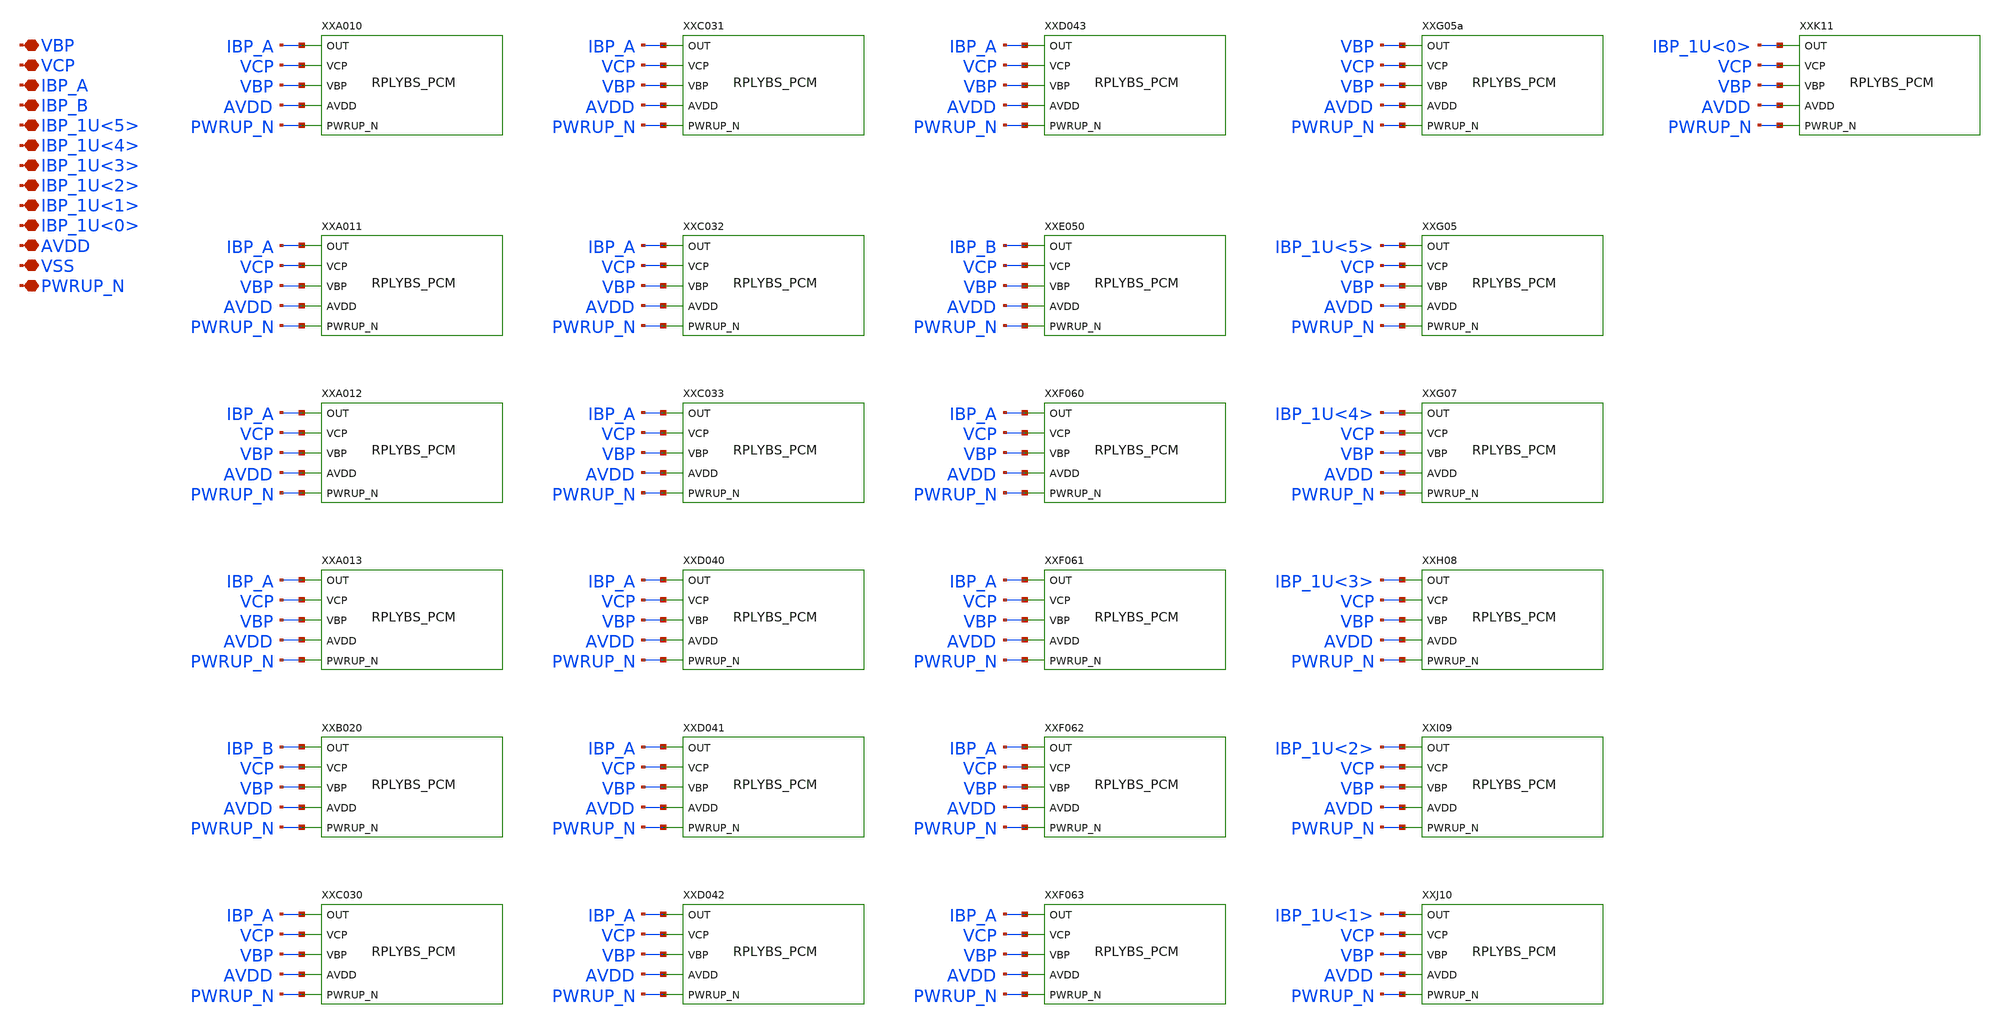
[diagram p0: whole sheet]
** sch_path: design/RPLY_BIAS_SKY130NM/RPLYBS_PMIRR.sch
**.subckt RPLYBS_PMIRR VBP VCP IBP_A IBP_B IBP_1U<5> IBP_1U<4> IBP_1U<3> IBP_1U<2> IBP_1U<1>
*+ IBP_1U<0> AVDD VSS PWRUP_N
*.iopin VBP
*.iopin VCP
*.iopin IBP_A
*.iopin IBP_B
*.iopin IBP_1U<5>
*.iopin IBP_1U<4>
*.iopin IBP_1U<3>
*.iopin IBP_1U<2>
*.iopin IBP_1U<1>
*.iopin IBP_1U<0>
*.iopin AVDD
*.iopin VSS
*.iopin PWRUP_N
XXA010 IBP_A VCP VBP AVDD PWRUP_N RPLYBS_PCM
XXA011 IBP_A VCP VBP AVDD PWRUP_N RPLYBS_PCM
XXA012 IBP_A VCP VBP AVDD PWRUP_N RPLYBS_PCM
XXA013 IBP_A VCP VBP AVDD PWRUP_N RPLYBS_PCM
XXB020 IBP_B VCP VBP AVDD PWRUP_N RPLYBS_PCM
XXC030 IBP_A VCP VBP AVDD PWRUP_N RPLYBS_PCM
XXC031 IBP_A VCP VBP AVDD PWRUP_N RPLYBS_PCM
XXC032 IBP_A VCP VBP AVDD PWRUP_N RPLYBS_PCM
XXC033 IBP_A VCP VBP AVDD PWRUP_N RPLYBS_PCM
XXD040 IBP_A VCP VBP AVDD PWRUP_N RPLYBS_PCM
XXD041 IBP_A VCP VBP AVDD PWRUP_N RPLYBS_PCM
XXD042 IBP_A VCP VBP AVDD PWRUP_N RPLYBS_PCM
XXD043 IBP_A VCP VBP AVDD PWRUP_N RPLYBS_PCM
XXE050 IBP_B VCP VBP AVDD PWRUP_N RPLYBS_PCM
XXF060 IBP_A VCP VBP AVDD PWRUP_N RPLYBS_PCM
XXF061 IBP_A VCP VBP AVDD PWRUP_N RPLYBS_PCM
XXF062 IBP_A VCP VBP AVDD PWRUP_N RPLYBS_PCM
XXF063 IBP_A VCP VBP AVDD PWRUP_N RPLYBS_PCM
XXG05a VBP VCP VBP AVDD PWRUP_N RPLYBS_PCM
XXG05 IBP_1U<5> VCP VBP AVDD PWRUP_N RPLYBS_PCM
XXG07 IBP_1U<4> VCP VBP AVDD PWRUP_N RPLYBS_PCM
XXH08 IBP_1U<3> VCP VBP AVDD PWRUP_N RPLYBS_PCM
XXI09 IBP_1U<2> VCP VBP AVDD PWRUP_N RPLYBS_PCM
XXJ10 IBP_1U<1> VCP VBP AVDD PWRUP_N RPLYBS_PCM
XXK11 IBP_1U<0> VCP VBP AVDD PWRUP_N RPLYBS_PCM
**.ends
.end
